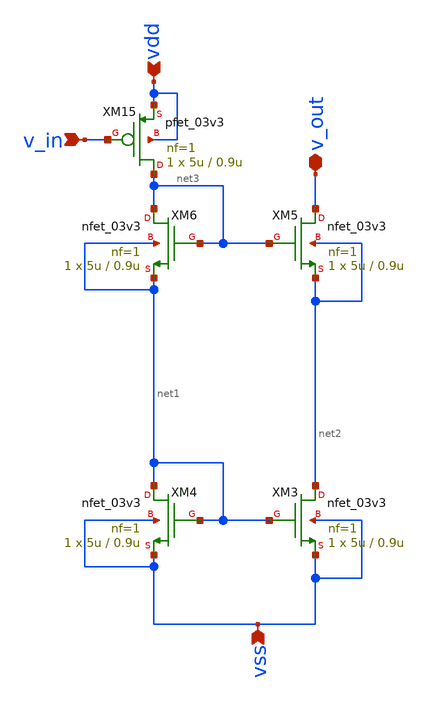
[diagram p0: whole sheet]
** sch_path: blocks/composite/regulated_cascoded_cmirror/xschem/biased_cm.sch
**.subckt biased_cm v_in vdd vss v_out
*.ipin v_in
*.ipin vdd
*.ipin vss
*.iopin v_out
XM3 net2 net1 vss vss nfet_03v3 L=0.9u W=5u nf=1 ad='int((nf+1)/2) * W/nf * 0.18u' as='int((nf+2)/2) * W/nf * 0.18u'
+ pd='2*int((nf+1)/2) * (W/nf + 0.18u)' ps='2*int((nf+2)/2) * (W/nf + 0.18u)' nrd='0.18u / W' nrs='0.18u / W'
+ sa=0 sb=0 sd=0 m=1
XM4 net1 net1 vss vss nfet_03v3 L=0.9u W=5u nf=1 ad='int((nf+1)/2) * W/nf * 0.18u' as='int((nf+2)/2) * W/nf * 0.18u'
+ pd='2*int((nf+1)/2) * (W/nf + 0.18u)' ps='2*int((nf+2)/2) * (W/nf + 0.18u)' nrd='0.18u / W' nrs='0.18u / W'
+ sa=0 sb=0 sd=0 m=1
XM5 v_out net3 net2 net2 nfet_03v3 L=0.9u W=5u nf=1 ad='int((nf+1)/2) * W/nf * 0.18u' as='int((nf+2)/2) * W/nf * 0.18u'
+ pd='2*int((nf+1)/2) * (W/nf + 0.18u)' ps='2*int((nf+2)/2) * (W/nf + 0.18u)' nrd='0.18u / W' nrs='0.18u / W'
+ sa=0 sb=0 sd=0 m=1
XM6 net3 net3 net1 net1 nfet_03v3 L=0.9u W=5u nf=1 ad='int((nf+1)/2) * W/nf * 0.18u' as='int((nf+2)/2) * W/nf * 0.18u'
+ pd='2*int((nf+1)/2) * (W/nf + 0.18u)' ps='2*int((nf+2)/2) * (W/nf + 0.18u)' nrd='0.18u / W' nrs='0.18u / W'
+ sa=0 sb=0 sd=0 m=1
XM15 net3 v_in vdd vdd pfet_03v3 L=0.9u W=5u nf=1 ad='int((nf+1)/2) * W/nf * 0.18u' as='int((nf+2)/2) * W/nf * 0.18u'
+ pd='2*int((nf+1)/2) * (W/nf + 0.18u)' ps='2*int((nf+2)/2) * (W/nf + 0.18u)' nrd='0.18u / W' nrs='0.18u / W'
+ sa=0 sb=0 sd=0 m=1
**.ends
.end
